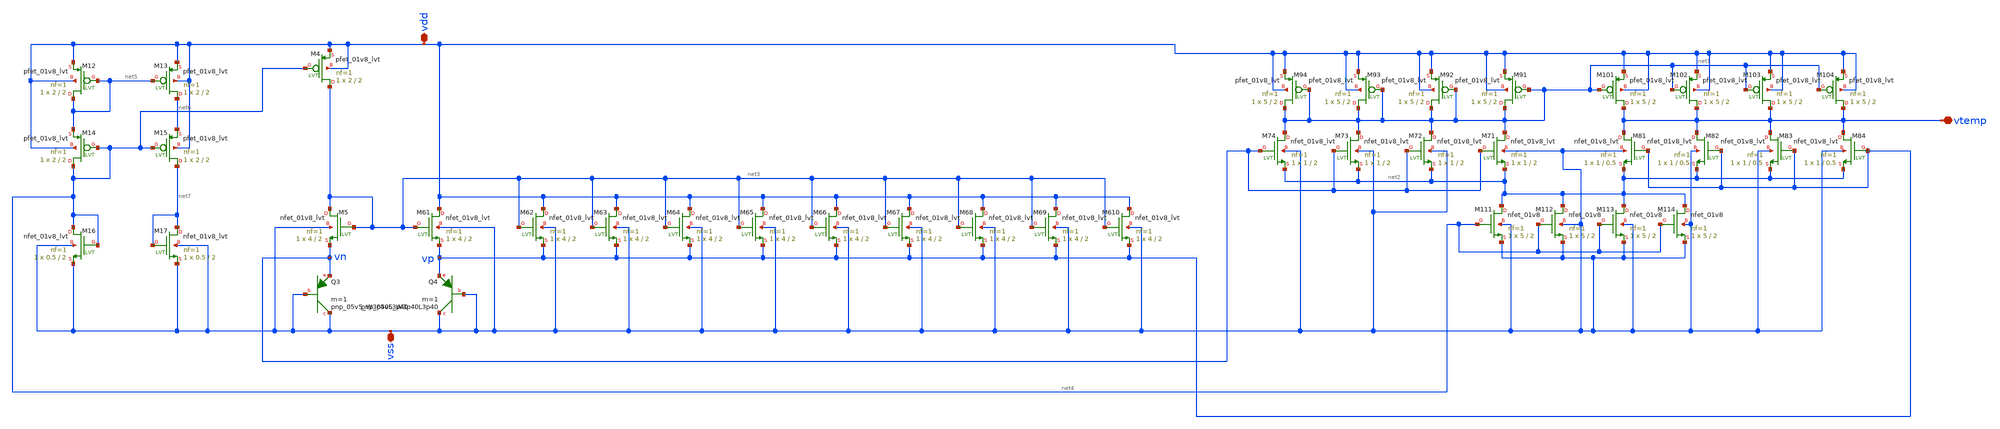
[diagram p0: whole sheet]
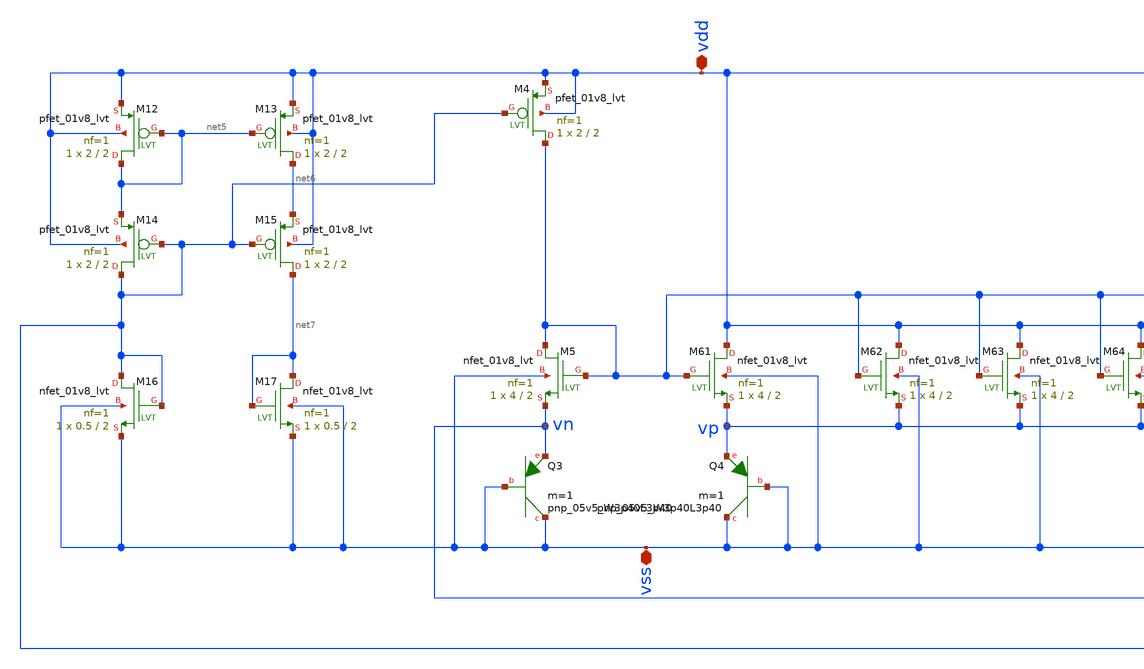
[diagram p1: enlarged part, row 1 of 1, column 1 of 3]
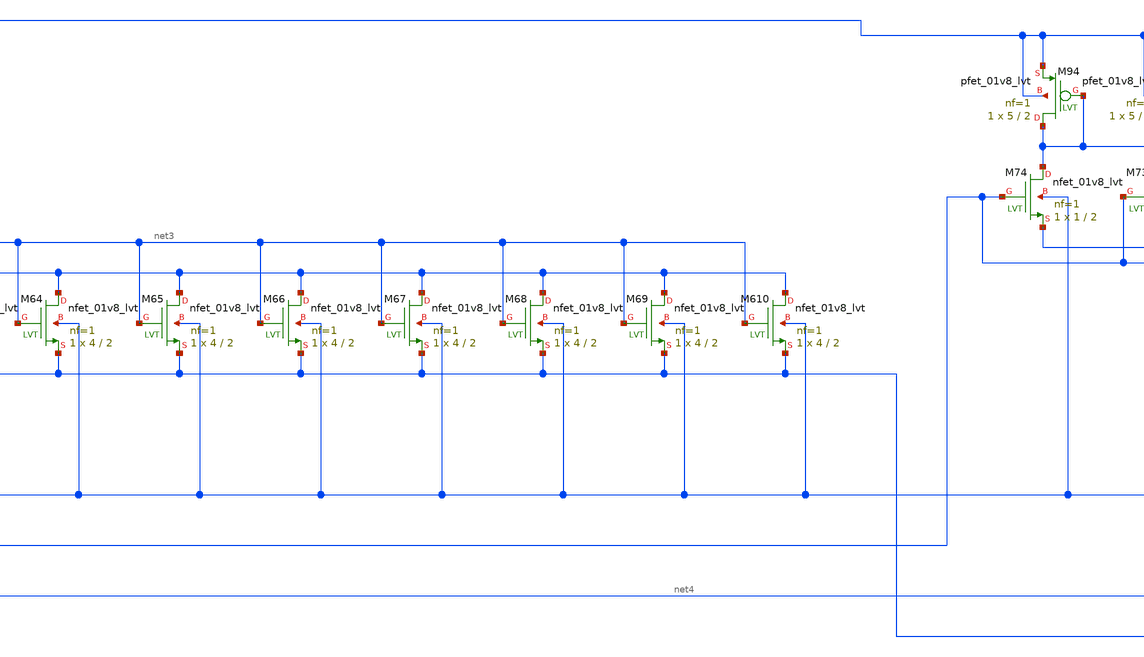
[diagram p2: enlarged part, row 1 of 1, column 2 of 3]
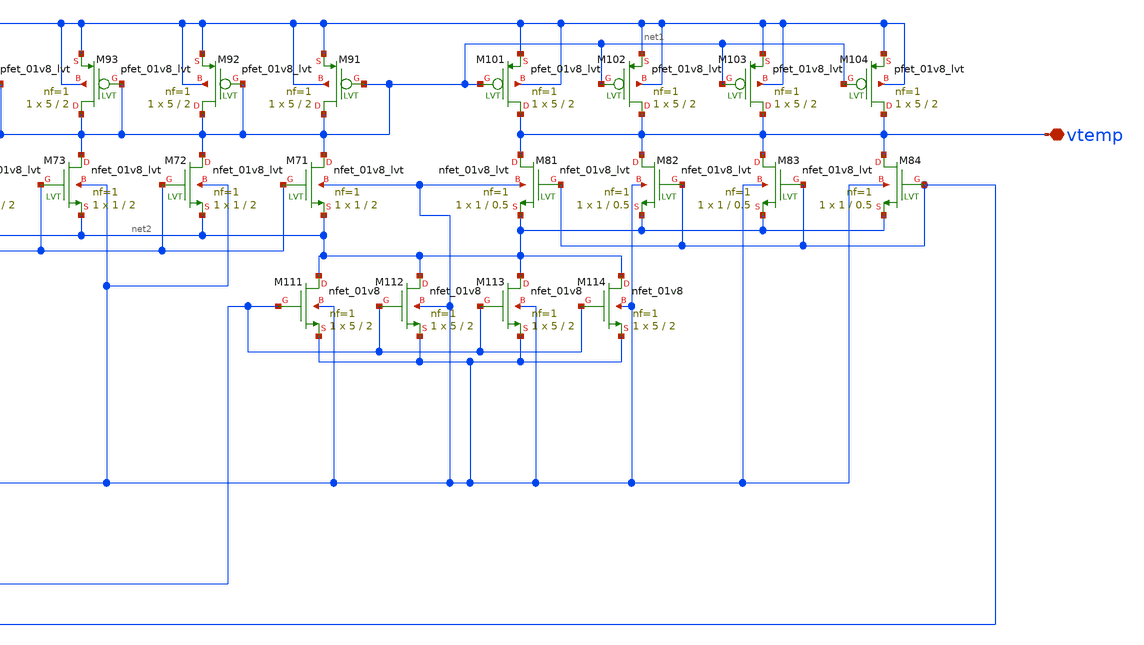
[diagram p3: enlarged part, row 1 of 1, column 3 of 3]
** sch_path: XSCHEM/For_Layout/Temperature_Sensor.sch
**.subckt Temperature_Sensor vdd vss vtemp
*.iopin vdd
*.iopin vss
*.iopin vtemp
XM71 net1 vn net2 vss sky130_fd_pr__nfet_01v8_lvt L=2 W=1 nf=1 ad='int((nf+1)/2) * W/nf * 0.29' as='int((nf+2)/2) * W/nf * 0.29'
+ pd='2*int((nf+1)/2) * (W/nf + 0.29)' ps='2*int((nf+2)/2) * (W/nf + 0.29)' nrd='0.29 / W' nrs='0.29 / W'
+ sa=0 sb=0 sd=0 mult=1 m=1
XM81 vtemp vp net2 vss sky130_fd_pr__nfet_01v8_lvt L=0.5 W=1 nf=1 ad='int((nf+1)/2) * W/nf * 0.29' as='int((nf+2)/2) * W/nf * 0.29'
+ pd='2*int((nf+1)/2) * (W/nf + 0.29)' ps='2*int((nf+2)/2) * (W/nf + 0.29)' nrd='0.29 / W' nrs='0.29 / W'
+ sa=0 sb=0 sd=0 mult=1 m=1
XM112 net2 net4 vss vss sky130_fd_pr__nfet_01v8 L=2 W=5 nf=1 ad='int((nf+1)/2) * W/nf * 0.29' as='int((nf+2)/2) * W/nf * 0.29'
+ pd='2*int((nf+1)/2) * (W/nf + 0.29)' ps='2*int((nf+2)/2) * (W/nf + 0.29)' nrd='0.29 / W' nrs='0.29 / W'
+ sa=0 sb=0 sd=0 mult=1 m=1
XM91 net1 net1 vdd vdd sky130_fd_pr__pfet_01v8_lvt L=2 W=5 nf=1 ad='int((nf+1)/2) * W/nf * 0.29' as='int((nf+2)/2) * W/nf * 0.29'
+ pd='2*int((nf+1)/2) * (W/nf + 0.29)' ps='2*int((nf+2)/2) * (W/nf + 0.29)' nrd='0.29 / W' nrs='0.29 / W'
+ sa=0 sb=0 sd=0 mult=1 m=1
XM101 vtemp net1 vdd vdd sky130_fd_pr__pfet_01v8_lvt L=2 W=5 nf=1 ad='int((nf+1)/2) * W/nf * 0.29' as='int((nf+2)/2) * W/nf * 0.29'
+ pd='2*int((nf+1)/2) * (W/nf + 0.29)' ps='2*int((nf+2)/2) * (W/nf + 0.29)' nrd='0.29 / W' nrs='0.29 / W'
+ sa=0 sb=0 sd=0 mult=1 m=1
XM5 net3 net3 vn vss sky130_fd_pr__nfet_01v8_lvt L=2 W=4 nf=1 ad='int((nf+1)/2) * W/nf * 0.29' as='int((nf+2)/2) * W/nf * 0.29'
+ pd='2*int((nf+1)/2) * (W/nf + 0.29)' ps='2*int((nf+2)/2) * (W/nf + 0.29)' nrd='0.29 / W' nrs='0.29 / W'
+ sa=0 sb=0 sd=0 mult=1 m=1
XQ3 vss vss vn sky130_fd_pr__pnp_05v5_W3p40L3p40 m=1
XM61 vdd net3 vp vss sky130_fd_pr__nfet_01v8_lvt L=2 W=4 nf=1 ad='int((nf+1)/2) * W/nf * 0.29' as='int((nf+2)/2) * W/nf * 0.29'
+ pd='2*int((nf+1)/2) * (W/nf + 0.29)' ps='2*int((nf+2)/2) * (W/nf + 0.29)' nrd='0.29 / W' nrs='0.29 / W'
+ sa=0 sb=0 sd=0 mult=1 m=1
XQ4 vss vss vp sky130_fd_pr__pnp_05v5_W3p40L3p40 m=1
XM4 net3 net4 vdd vdd sky130_fd_pr__pfet_01v8_lvt L=2 W=2 nf=1 ad='int((nf+1)/2) * W/nf * 0.29' as='int((nf+2)/2) * W/nf * 0.29'
+ pd='2*int((nf+1)/2) * (W/nf + 0.29)' ps='2*int((nf+2)/2) * (W/nf + 0.29)' nrd='0.29 / W' nrs='0.29 / W'
+ sa=0 sb=0 sd=0 mult=1 m=1
XM62 vdd net3 vp vss sky130_fd_pr__nfet_01v8_lvt L=2 W=4 nf=1 ad='int((nf+1)/2) * W/nf * 0.29' as='int((nf+2)/2) * W/nf * 0.29'
+ pd='2*int((nf+1)/2) * (W/nf + 0.29)' ps='2*int((nf+2)/2) * (W/nf + 0.29)' nrd='0.29 / W' nrs='0.29 / W'
+ sa=0 sb=0 sd=0 mult=1 m=1
XM63 vdd net3 vp vss sky130_fd_pr__nfet_01v8_lvt L=2 W=4 nf=1 ad='int((nf+1)/2) * W/nf * 0.29' as='int((nf+2)/2) * W/nf * 0.29'
+ pd='2*int((nf+1)/2) * (W/nf + 0.29)' ps='2*int((nf+2)/2) * (W/nf + 0.29)' nrd='0.29 / W' nrs='0.29 / W'
+ sa=0 sb=0 sd=0 mult=1 m=1
XM64 vdd net3 vp vss sky130_fd_pr__nfet_01v8_lvt L=2 W=4 nf=1 ad='int((nf+1)/2) * W/nf * 0.29' as='int((nf+2)/2) * W/nf * 0.29'
+ pd='2*int((nf+1)/2) * (W/nf + 0.29)' ps='2*int((nf+2)/2) * (W/nf + 0.29)' nrd='0.29 / W' nrs='0.29 / W'
+ sa=0 sb=0 sd=0 mult=1 m=1
XM65 vdd net3 vp vss sky130_fd_pr__nfet_01v8_lvt L=2 W=4 nf=1 ad='int((nf+1)/2) * W/nf * 0.29' as='int((nf+2)/2) * W/nf * 0.29'
+ pd='2*int((nf+1)/2) * (W/nf + 0.29)' ps='2*int((nf+2)/2) * (W/nf + 0.29)' nrd='0.29 / W' nrs='0.29 / W'
+ sa=0 sb=0 sd=0 mult=1 m=1
XM66 vdd net3 vp vss sky130_fd_pr__nfet_01v8_lvt L=2 W=4 nf=1 ad='int((nf+1)/2) * W/nf * 0.29' as='int((nf+2)/2) * W/nf * 0.29'
+ pd='2*int((nf+1)/2) * (W/nf + 0.29)' ps='2*int((nf+2)/2) * (W/nf + 0.29)' nrd='0.29 / W' nrs='0.29 / W'
+ sa=0 sb=0 sd=0 mult=1 m=1
XM67 vdd net3 vp vss sky130_fd_pr__nfet_01v8_lvt L=2 W=4 nf=1 ad='int((nf+1)/2) * W/nf * 0.29' as='int((nf+2)/2) * W/nf * 0.29'
+ pd='2*int((nf+1)/2) * (W/nf + 0.29)' ps='2*int((nf+2)/2) * (W/nf + 0.29)' nrd='0.29 / W' nrs='0.29 / W'
+ sa=0 sb=0 sd=0 mult=1 m=1
XM68 vdd net3 vp vss sky130_fd_pr__nfet_01v8_lvt L=2 W=4 nf=1 ad='int((nf+1)/2) * W/nf * 0.29' as='int((nf+2)/2) * W/nf * 0.29'
+ pd='2*int((nf+1)/2) * (W/nf + 0.29)' ps='2*int((nf+2)/2) * (W/nf + 0.29)' nrd='0.29 / W' nrs='0.29 / W'
+ sa=0 sb=0 sd=0 mult=1 m=1
XM69 vdd net3 vp vss sky130_fd_pr__nfet_01v8_lvt L=2 W=4 nf=1 ad='int((nf+1)/2) * W/nf * 0.29' as='int((nf+2)/2) * W/nf * 0.29'
+ pd='2*int((nf+1)/2) * (W/nf + 0.29)' ps='2*int((nf+2)/2) * (W/nf + 0.29)' nrd='0.29 / W' nrs='0.29 / W'
+ sa=0 sb=0 sd=0 mult=1 m=1
XM610 vdd net3 vp vss sky130_fd_pr__nfet_01v8_lvt L=2 W=4 nf=1 ad='int((nf+1)/2) * W/nf * 0.29' as='int((nf+2)/2) * W/nf * 0.29'
+ pd='2*int((nf+1)/2) * (W/nf + 0.29)' ps='2*int((nf+2)/2) * (W/nf + 0.29)' nrd='0.29 / W' nrs='0.29 / W'
+ sa=0 sb=0 sd=0 mult=1 m=1
XM92 net1 net1 vdd vdd sky130_fd_pr__pfet_01v8_lvt L=2 W=5 nf=1 ad='int((nf+1)/2) * W/nf * 0.29' as='int((nf+2)/2) * W/nf * 0.29'
+ pd='2*int((nf+1)/2) * (W/nf + 0.29)' ps='2*int((nf+2)/2) * (W/nf + 0.29)' nrd='0.29 / W' nrs='0.29 / W'
+ sa=0 sb=0 sd=0 mult=1 m=1
XM93 net1 net1 vdd vdd sky130_fd_pr__pfet_01v8_lvt L=2 W=5 nf=1 ad='int((nf+1)/2) * W/nf * 0.29' as='int((nf+2)/2) * W/nf * 0.29'
+ pd='2*int((nf+1)/2) * (W/nf + 0.29)' ps='2*int((nf+2)/2) * (W/nf + 0.29)' nrd='0.29 / W' nrs='0.29 / W'
+ sa=0 sb=0 sd=0 mult=1 m=1
XM94 net1 net1 vdd vdd sky130_fd_pr__pfet_01v8_lvt L=2 W=5 nf=1 ad='int((nf+1)/2) * W/nf * 0.29' as='int((nf+2)/2) * W/nf * 0.29'
+ pd='2*int((nf+1)/2) * (W/nf + 0.29)' ps='2*int((nf+2)/2) * (W/nf + 0.29)' nrd='0.29 / W' nrs='0.29 / W'
+ sa=0 sb=0 sd=0 mult=1 m=1
XM102 vtemp net1 vdd vdd sky130_fd_pr__pfet_01v8_lvt L=2 W=5 nf=1 ad='int((nf+1)/2) * W/nf * 0.29' as='int((nf+2)/2) * W/nf * 0.29'
+ pd='2*int((nf+1)/2) * (W/nf + 0.29)' ps='2*int((nf+2)/2) * (W/nf + 0.29)' nrd='0.29 / W' nrs='0.29 / W'
+ sa=0 sb=0 sd=0 mult=1 m=1
XM103 vtemp net1 vdd vdd sky130_fd_pr__pfet_01v8_lvt L=2 W=5 nf=1 ad='int((nf+1)/2) * W/nf * 0.29' as='int((nf+2)/2) * W/nf * 0.29'
+ pd='2*int((nf+1)/2) * (W/nf + 0.29)' ps='2*int((nf+2)/2) * (W/nf + 0.29)' nrd='0.29 / W' nrs='0.29 / W'
+ sa=0 sb=0 sd=0 mult=1 m=1
XM104 vtemp net1 vdd vdd sky130_fd_pr__pfet_01v8_lvt L=2 W=5 nf=1 ad='int((nf+1)/2) * W/nf * 0.29' as='int((nf+2)/2) * W/nf * 0.29'
+ pd='2*int((nf+1)/2) * (W/nf + 0.29)' ps='2*int((nf+2)/2) * (W/nf + 0.29)' nrd='0.29 / W' nrs='0.29 / W'
+ sa=0 sb=0 sd=0 mult=1 m=1
XM72 net1 vn net2 vss sky130_fd_pr__nfet_01v8_lvt L=2 W=1 nf=1 ad='int((nf+1)/2) * W/nf * 0.29' as='int((nf+2)/2) * W/nf * 0.29'
+ pd='2*int((nf+1)/2) * (W/nf + 0.29)' ps='2*int((nf+2)/2) * (W/nf + 0.29)' nrd='0.29 / W' nrs='0.29 / W'
+ sa=0 sb=0 sd=0 mult=1 m=1
XM73 net1 vn net2 vss sky130_fd_pr__nfet_01v8_lvt L=2 W=1 nf=1 ad='int((nf+1)/2) * W/nf * 0.29' as='int((nf+2)/2) * W/nf * 0.29'
+ pd='2*int((nf+1)/2) * (W/nf + 0.29)' ps='2*int((nf+2)/2) * (W/nf + 0.29)' nrd='0.29 / W' nrs='0.29 / W'
+ sa=0 sb=0 sd=0 mult=1 m=1
XM74 net1 vn net2 vss sky130_fd_pr__nfet_01v8_lvt L=2 W=1 nf=1 ad='int((nf+1)/2) * W/nf * 0.29' as='int((nf+2)/2) * W/nf * 0.29'
+ pd='2*int((nf+1)/2) * (W/nf + 0.29)' ps='2*int((nf+2)/2) * (W/nf + 0.29)' nrd='0.29 / W' nrs='0.29 / W'
+ sa=0 sb=0 sd=0 mult=1 m=1
XM82 vtemp vp net2 vss sky130_fd_pr__nfet_01v8_lvt L=0.5 W=1 nf=1 ad='int((nf+1)/2) * W/nf * 0.29' as='int((nf+2)/2) * W/nf * 0.29'
+ pd='2*int((nf+1)/2) * (W/nf + 0.29)' ps='2*int((nf+2)/2) * (W/nf + 0.29)' nrd='0.29 / W' nrs='0.29 / W'
+ sa=0 sb=0 sd=0 mult=1 m=1
XM83 vtemp vp net2 vss sky130_fd_pr__nfet_01v8_lvt L=0.5 W=1 nf=1 ad='int((nf+1)/2) * W/nf * 0.29' as='int((nf+2)/2) * W/nf * 0.29'
+ pd='2*int((nf+1)/2) * (W/nf + 0.29)' ps='2*int((nf+2)/2) * (W/nf + 0.29)' nrd='0.29 / W' nrs='0.29 / W'
+ sa=0 sb=0 sd=0 mult=1 m=1
XM84 vtemp vp net2 vss sky130_fd_pr__nfet_01v8_lvt L=0.5 W=1 nf=1 ad='int((nf+1)/2) * W/nf * 0.29' as='int((nf+2)/2) * W/nf * 0.29'
+ pd='2*int((nf+1)/2) * (W/nf + 0.29)' ps='2*int((nf+2)/2) * (W/nf + 0.29)' nrd='0.29 / W' nrs='0.29 / W'
+ sa=0 sb=0 sd=0 mult=1 m=1
XM111 net2 net4 vss vss sky130_fd_pr__nfet_01v8 L=2 W=5 nf=1 ad='int((nf+1)/2) * W/nf * 0.29' as='int((nf+2)/2) * W/nf * 0.29'
+ pd='2*int((nf+1)/2) * (W/nf + 0.29)' ps='2*int((nf+2)/2) * (W/nf + 0.29)' nrd='0.29 / W' nrs='0.29 / W'
+ sa=0 sb=0 sd=0 mult=1 m=1
XM113 net2 net4 vss vss sky130_fd_pr__nfet_01v8 L=2 W=5 nf=1 ad='int((nf+1)/2) * W/nf * 0.29' as='int((nf+2)/2) * W/nf * 0.29'
+ pd='2*int((nf+1)/2) * (W/nf + 0.29)' ps='2*int((nf+2)/2) * (W/nf + 0.29)' nrd='0.29 / W' nrs='0.29 / W'
+ sa=0 sb=0 sd=0 mult=1 m=1
XM114 net2 net4 vss vss sky130_fd_pr__nfet_01v8 L=2 W=5 nf=1 ad='int((nf+1)/2) * W/nf * 0.29' as='int((nf+2)/2) * W/nf * 0.29'
+ pd='2*int((nf+1)/2) * (W/nf + 0.29)' ps='2*int((nf+2)/2) * (W/nf + 0.29)' nrd='0.29 / W' nrs='0.29 / W'
+ sa=0 sb=0 sd=0 mult=1 m=1
XM12 net5 net5 vdd vdd sky130_fd_pr__pfet_01v8_lvt L=2 W=2 nf=1 ad='int((nf+1)/2) * W/nf * 0.29' as='int((nf+2)/2) * W/nf * 0.29'
+ pd='2*int((nf+1)/2) * (W/nf + 0.29)' ps='2*int((nf+2)/2) * (W/nf + 0.29)' nrd='0.29 / W' nrs='0.29 / W'
+ sa=0 sb=0 sd=0 mult=1 m=1
XM16 net4 net4 vss vss sky130_fd_pr__nfet_01v8_lvt L=2 W=0.5 nf=1 ad='int((nf+1)/2) * W/nf * 0.29' as='int((nf+2)/2) * W/nf * 0.29'
+ pd='2*int((nf+1)/2) * (W/nf + 0.29)' ps='2*int((nf+2)/2) * (W/nf + 0.29)' nrd='0.29 / W' nrs='0.29 / W'
+ sa=0 sb=0 sd=0 mult=1 m=1
XM13 net6 net5 vdd vdd sky130_fd_pr__pfet_01v8_lvt L=2 W=2 nf=1 ad='int((nf+1)/2) * W/nf * 0.29' as='int((nf+2)/2) * W/nf * 0.29'
+ pd='2*int((nf+1)/2) * (W/nf + 0.29)' ps='2*int((nf+2)/2) * (W/nf + 0.29)' nrd='0.29 / W' nrs='0.29 / W'
+ sa=0 sb=0 sd=0 mult=1 m=1
XM15 net7 net4 net6 vdd sky130_fd_pr__pfet_01v8_lvt L=2 W=2 nf=1 ad='int((nf+1)/2) * W/nf * 0.29' as='int((nf+2)/2) * W/nf * 0.29'
+ pd='2*int((nf+1)/2) * (W/nf + 0.29)' ps='2*int((nf+2)/2) * (W/nf + 0.29)' nrd='0.29 / W' nrs='0.29 / W'
+ sa=0 sb=0 sd=0 mult=1 m=1
XM14 net4 net4 net5 vdd sky130_fd_pr__pfet_01v8_lvt L=2 W=2 nf=1 ad='int((nf+1)/2) * W/nf * 0.29' as='int((nf+2)/2) * W/nf * 0.29'
+ pd='2*int((nf+1)/2) * (W/nf + 0.29)' ps='2*int((nf+2)/2) * (W/nf + 0.29)' nrd='0.29 / W' nrs='0.29 / W'
+ sa=0 sb=0 sd=0 mult=1 m=1
XM17 net7 net7 vss vss sky130_fd_pr__nfet_01v8_lvt L=2 W=0.5 nf=1 ad='int((nf+1)/2) * W/nf * 0.29' as='int((nf+2)/2) * W/nf * 0.29'
+ pd='2*int((nf+1)/2) * (W/nf + 0.29)' ps='2*int((nf+2)/2) * (W/nf + 0.29)' nrd='0.29 / W' nrs='0.29 / W'
+ sa=0 sb=0 sd=0 mult=1 m=1
**.ends
.end
